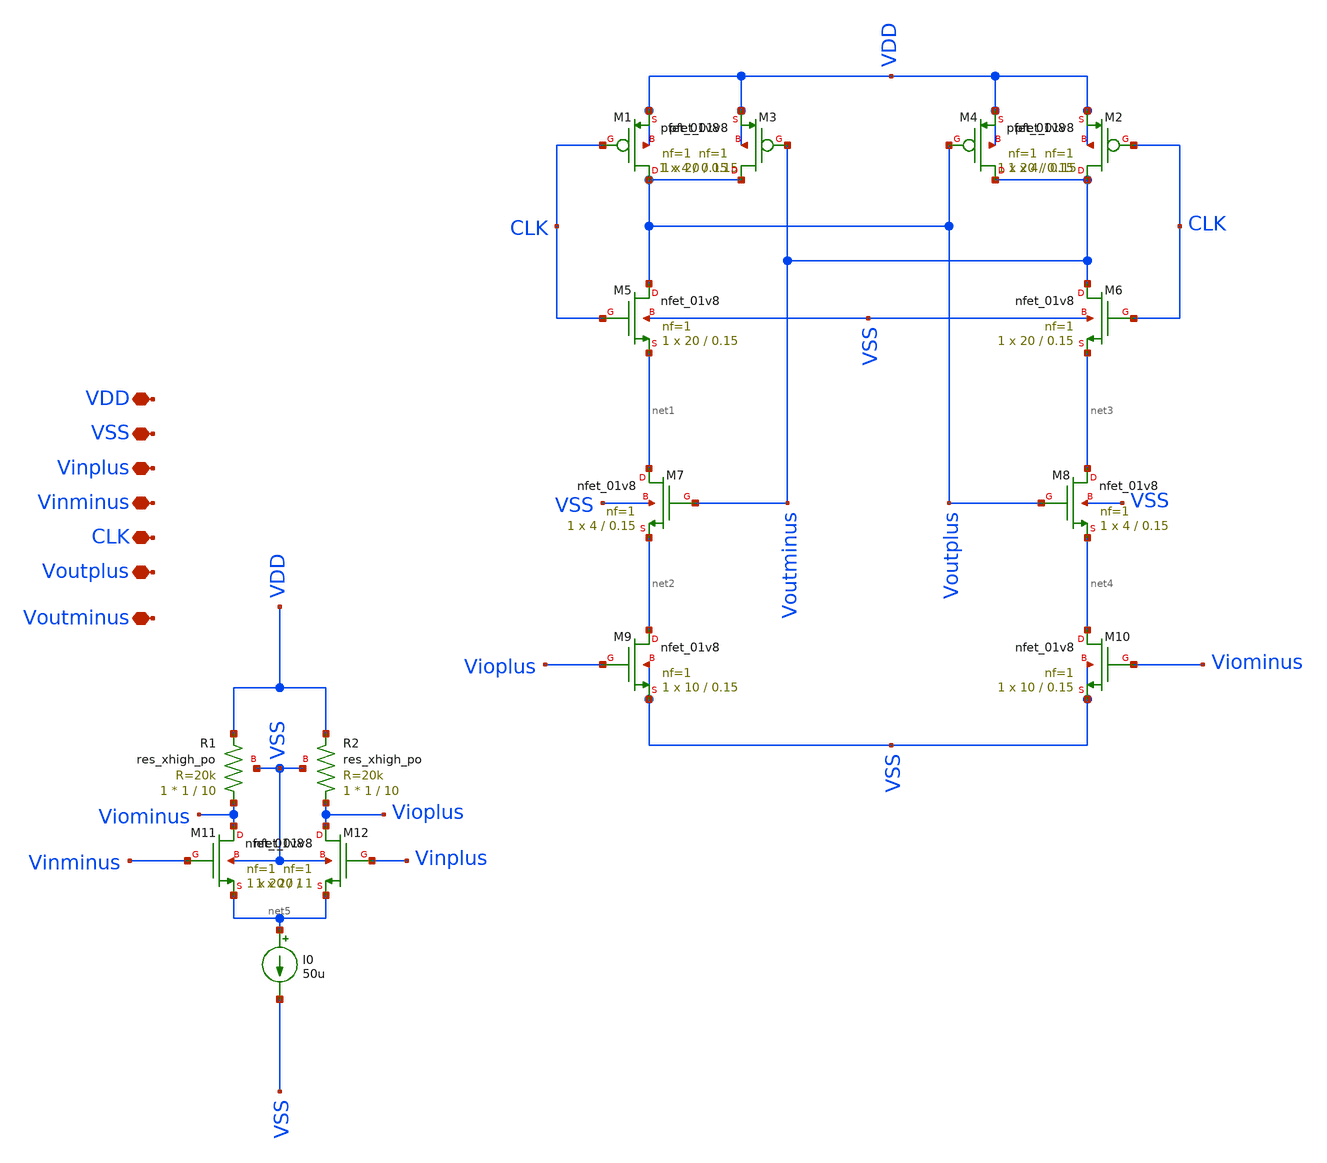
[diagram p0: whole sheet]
** sch_path: xschem/to_send/Comparator.sch
**.subckt Comparator VDD VSS Vinplus Vinminus CLK Voutplus Voutminus
*.iopin VDD
*.iopin VSS
*.iopin Vinplus
*.iopin Vinminus
*.iopin CLK
*.iopin Voutplus
*.iopin Voutminus
XM1 Voutplus CLK VDD VDD sky130_fd_pr__pfet_01v8 L=0.15 W=20 nf=1 ad='int((nf+1)/2) * W/nf * 0.29' as='int((nf+2)/2) * W/nf * 0.29'
+ pd='2*int((nf+1)/2) * (W/nf + 0.29)' ps='2*int((nf+2)/2) * (W/nf + 0.29)' nrd='0.29 / W' nrs='0.29 / W'
+ sa=0 sb=0 sd=0 mult=1 m=1
XM2 Voutminus CLK VDD VDD sky130_fd_pr__pfet_01v8 L=0.15 W=20 nf=1 ad='int((nf+1)/2) * W/nf * 0.29' as='int((nf+2)/2) * W/nf * 0.29'
+ pd='2*int((nf+1)/2) * (W/nf + 0.29)' ps='2*int((nf+2)/2) * (W/nf + 0.29)' nrd='0.29 / W' nrs='0.29 / W'
+ sa=0 sb=0 sd=0 mult=1 m=1
XM3 Voutplus Voutminus VDD VDD sky130_fd_pr__pfet_01v8 L=0.15 W=4 nf=1 ad='int((nf+1)/2) * W/nf * 0.29'
+ as='int((nf+2)/2) * W/nf * 0.29' pd='2*int((nf+1)/2) * (W/nf + 0.29)' ps='2*int((nf+2)/2) * (W/nf + 0.29)'
+ nrd='0.29 / W' nrs='0.29 / W' sa=0 sb=0 sd=0 mult=1 m=1
XM4 Voutminus Voutplus VDD VDD sky130_fd_pr__pfet_01v8 L=0.15 W=4 nf=1 ad='int((nf+1)/2) * W/nf * 0.29'
+ as='int((nf+2)/2) * W/nf * 0.29' pd='2*int((nf+1)/2) * (W/nf + 0.29)' ps='2*int((nf+2)/2) * (W/nf + 0.29)'
+ nrd='0.29 / W' nrs='0.29 / W' sa=0 sb=0 sd=0 mult=1 m=1
XM5 Voutplus CLK net1 VSS sky130_fd_pr__nfet_01v8 L=0.15 W=20 nf=1 ad='int((nf+1)/2) * W/nf * 0.29' as='int((nf+2)/2) * W/nf * 0.29'
+ pd='2*int((nf+1)/2) * (W/nf + 0.29)' ps='2*int((nf+2)/2) * (W/nf + 0.29)' nrd='0.29 / W' nrs='0.29 / W'
+ sa=0 sb=0 sd=0 mult=1 m=1
XM6 Voutminus CLK net3 VSS sky130_fd_pr__nfet_01v8 L=0.15 W=20 nf=1 ad='int((nf+1)/2) * W/nf * 0.29'
+ as='int((nf+2)/2) * W/nf * 0.29' pd='2*int((nf+1)/2) * (W/nf + 0.29)' ps='2*int((nf+2)/2) * (W/nf + 0.29)'
+ nrd='0.29 / W' nrs='0.29 / W' sa=0 sb=0 sd=0 mult=1 m=1
XM7 net1 Voutminus net2 VSS sky130_fd_pr__nfet_01v8 L=0.15 W=4 nf=1 ad='int((nf+1)/2) * W/nf * 0.29'
+ as='int((nf+2)/2) * W/nf * 0.29' pd='2*int((nf+1)/2) * (W/nf + 0.29)' ps='2*int((nf+2)/2) * (W/nf + 0.29)'
+ nrd='0.29 / W' nrs='0.29 / W' sa=0 sb=0 sd=0 mult=1 m=1
XM8 net3 Voutplus net4 VSS sky130_fd_pr__nfet_01v8 L=0.15 W=4 nf=1 ad='int((nf+1)/2) * W/nf * 0.29' as='int((nf+2)/2) * W/nf * 0.29'
+ pd='2*int((nf+1)/2) * (W/nf + 0.29)' ps='2*int((nf+2)/2) * (W/nf + 0.29)' nrd='0.29 / W' nrs='0.29 / W'
+ sa=0 sb=0 sd=0 mult=1 m=1
XM9 net2 Vioplus VSS VSS sky130_fd_pr__nfet_01v8 L=0.15 W=10 nf=1 ad='int((nf+1)/2) * W/nf * 0.29' as='int((nf+2)/2) * W/nf * 0.29'
+ pd='2*int((nf+1)/2) * (W/nf + 0.29)' ps='2*int((nf+2)/2) * (W/nf + 0.29)' nrd='0.29 / W' nrs='0.29 / W'
+ sa=0 sb=0 sd=0 mult=1 m=1
XM10 net4 Viominus VSS VSS sky130_fd_pr__nfet_01v8 L=0.15 W=10 nf=1 ad='int((nf+1)/2) * W/nf * 0.29'
+ as='int((nf+2)/2) * W/nf * 0.29' pd='2*int((nf+1)/2) * (W/nf + 0.29)' ps='2*int((nf+2)/2) * (W/nf + 0.29)'
+ nrd='0.29 / W' nrs='0.29 / W' sa=0 sb=0 sd=0 mult=1 m=1
XM11 Viominus Vinminus net5 VSS sky130_fd_pr__nfet_01v8 L=1 W=20 nf=1 ad='int((nf+1)/2) * W/nf * 0.29'
+ as='int((nf+2)/2) * W/nf * 0.29' pd='2*int((nf+1)/2) * (W/nf + 0.29)' ps='2*int((nf+2)/2) * (W/nf + 0.29)'
+ nrd='0.29 / W' nrs='0.29 / W' sa=0 sb=0 sd=0 mult=1 m=1
XM12 Vioplus Vinplus net5 VSS sky130_fd_pr__nfet_01v8 L=1 W=20 nf=1 ad='int((nf+1)/2) * W/nf * 0.29'
+ as='int((nf+2)/2) * W/nf * 0.29' pd='2*int((nf+1)/2) * (W/nf + 0.29)' ps='2*int((nf+2)/2) * (W/nf + 0.29)'
+ nrd='0.29 / W' nrs='0.29 / W' sa=0 sb=0 sd=0 mult=1 m=1
I0 net5 VSS 50u
XR1 Viominus VDD VSS sky130_fd_pr__res_xhigh_po W=1 L=10 mult=1 m=1
XR2 Vioplus VDD VSS sky130_fd_pr__res_xhigh_po W=1 L=10 mult=1 m=1
**.ends
.end
